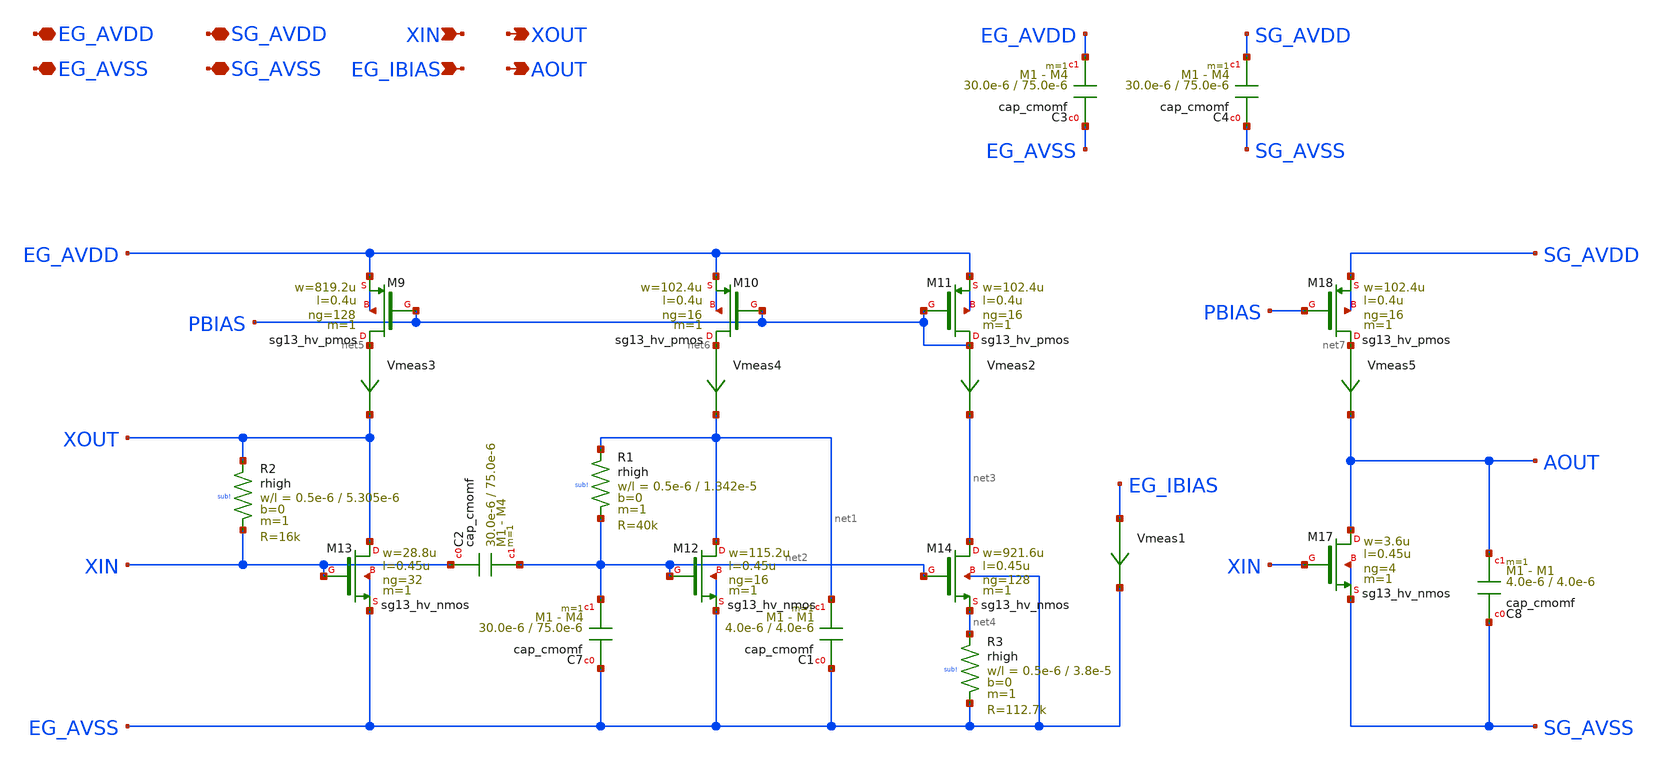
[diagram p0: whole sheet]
** sch_path: xschem/vittoz_pierce_osc_alt.sch
**.subckt vittoz_pierce_osc_alt EG_AVDD EG_AVSS SG_AVDD SG_AVSS XIN EG_IBIAS XOUT AOUT
*.iopin EG_AVDD
*.iopin EG_AVSS
*.iopin SG_AVDD
*.iopin SG_AVSS
*.ipin XIN
*.ipin EG_IBIAS
*.opin XOUT
*.opin AOUT
Vmeas3 net5 XOUT 0
.save i(vmeas3)
Vmeas4 net6 net1 0
.save i(vmeas4)
Vmeas2 PBIAS net3 0
.save i(vmeas2)
Vmeas5 net7 AOUT 0
.save i(vmeas5)
Vmeas1 EG_IBIAS EG_AVSS 0
.save i(vmeas1)
XC3 EG_AVSS EG_AVDD cap_cmomf w=30.0e-6 l=75.0e-6 mmin=1 mmax=4 subblock=0 rfmodel=0 subscale=1 m=1
+ mm_ok=1
XC4 SG_AVSS SG_AVDD cap_cmomf w=30.0e-6 l=75.0e-6 mmin=1 mmax=4 subblock=0 rfmodel=0 subscale=1 m=1
+ mm_ok=1
XR1 net1 net2 sub! rhigh w=0.5e-6 l=1.342e-5 m=1 b=0 mm_ok=1
XR2 XOUT XIN sub! rhigh w=0.5e-6 l=5.305e-6 m=1 b=0 mm_ok=1
XC2 XIN net2 cap_cmomf w=30.0e-6 l=75.0e-6 mmin=1 mmax=4 subblock=0 rfmodel=0 subscale=1 m=1 mm_ok=1
XC7 EG_AVSS net2 cap_cmomf w=30.0e-6 l=75.0e-6 mmin=1 mmax=4 subblock=0 rfmodel=0 subscale=1 m=1
+ mm_ok=1
XC1 EG_AVSS net1 cap_cmomf w=4.0e-6 l=4.0e-6 mmin=1 mmax=1 subblock=0 rfmodel=0 subscale=1 m=1
+ mm_ok=1
XC8 SG_AVSS AOUT cap_cmomf w=4.0e-6 l=4.0e-6 mmin=1 mmax=1 subblock=0 rfmodel=0 subscale=1 m=1
+ mm_ok=1
XM11 PBIAS PBIAS EG_AVDD EG_AVDD sg13_hv_pmos w=102.4u l=0.4u ng=16 m=1 mm_ok=1
XM10 net6 PBIAS EG_AVDD EG_AVDD sg13_hv_pmos w=102.4u l=0.4u ng=16 m=1 mm_ok=1
XM9 net5 PBIAS EG_AVDD EG_AVDD sg13_hv_pmos w=819.2u l=0.4u ng=128 m=1 mm_ok=1
XM14 net3 net2 net4 EG_AVSS sg13_hv_nmos w=921.6u l=0.45u ng=128 m=1 mm_ok=1
XM12 net1 net2 EG_AVSS EG_AVSS sg13_hv_nmos w=115.2u l=0.45u ng=16 m=1 mm_ok=1
XM13 XOUT XIN EG_AVSS EG_AVSS sg13_hv_nmos w=28.8u l=0.45u ng=32 m=1 mm_ok=1
XM18 net7 PBIAS SG_AVDD SG_AVDD sg13_hv_pmos w=102.4u l=0.4u ng=16 m=1 mm_ok=1
XM17 AOUT XIN SG_AVSS SG_AVSS sg13_hv_nmos w=3.6u l=0.45u ng=4 m=1 mm_ok=1
XR3 net4 EG_AVSS sub! rhigh w=0.5e-6 l=3.8e-5 m=1 b=0 mm_ok=1
**.ends
.end
